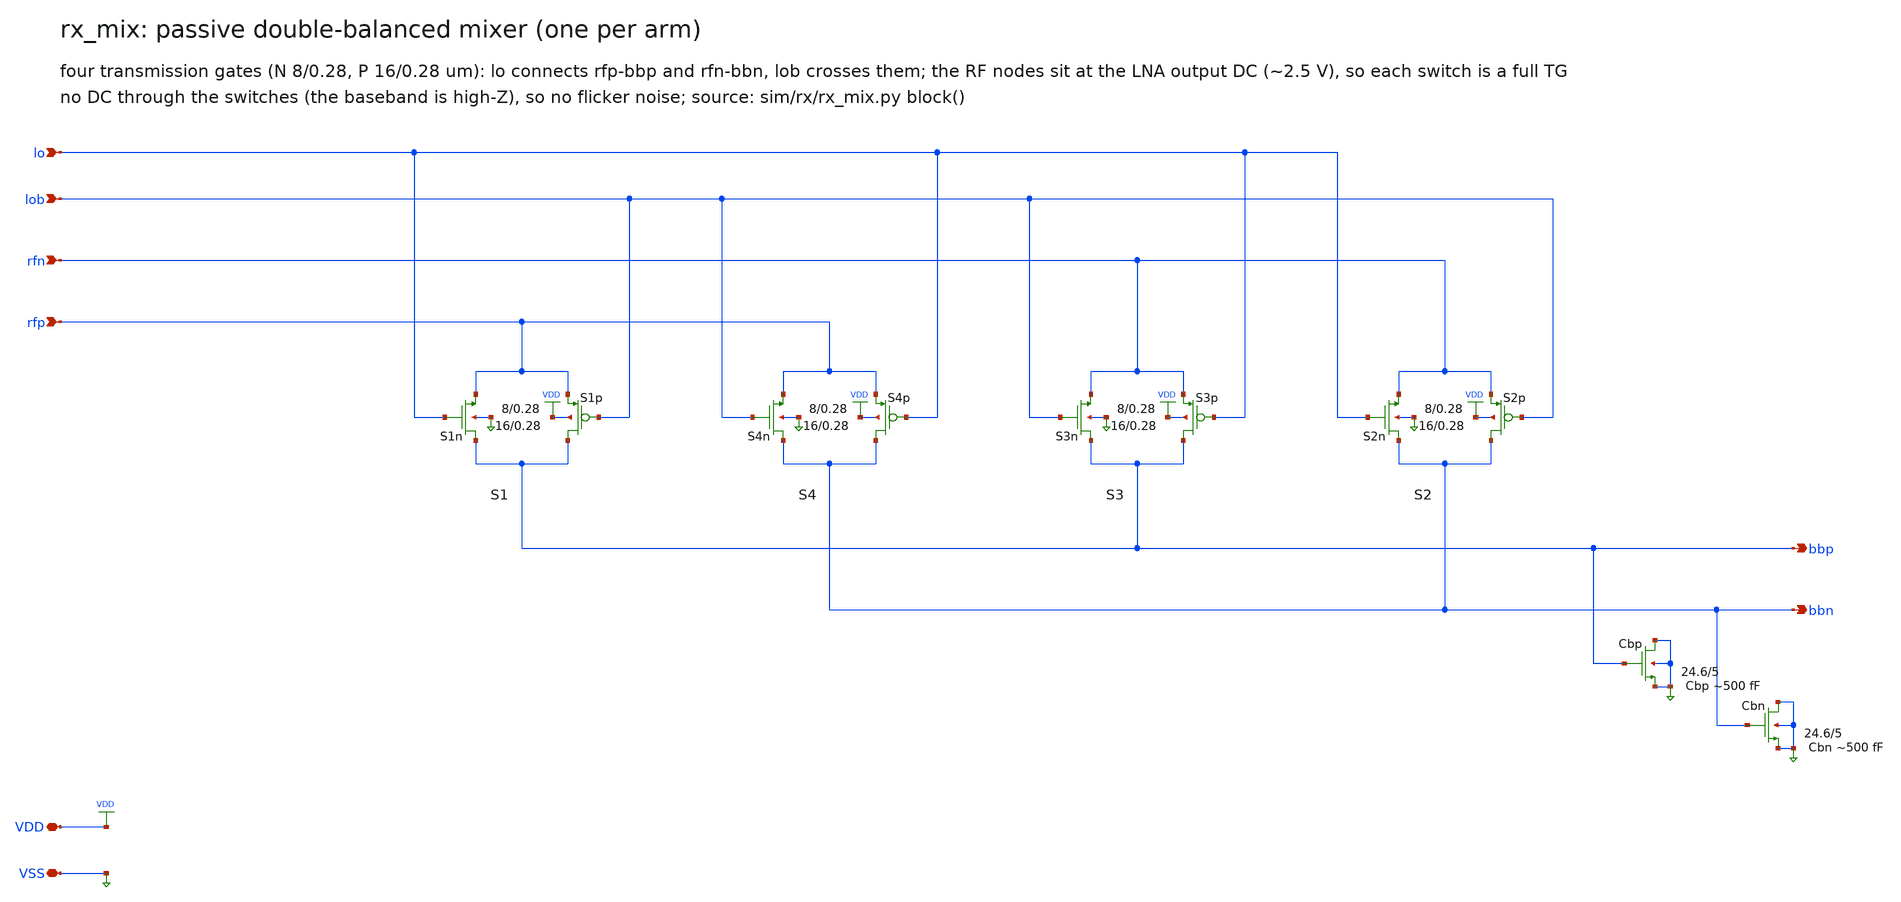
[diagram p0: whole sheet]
** sch_path: xschem/rx_mix.sch
**.subckt rx_mix VDD VSS rfp rfn bbp bbn lo lob
*.iopin VDD
*.iopin VSS
*.ipin rfp
*.ipin rfn
*.opin bbp
*.opin bbn
*.ipin lo
*.ipin lob
XS1n bbp lo rfp VSS nfet_03v3 L=0.28u W=8.0u nf=1 ad=4.0p as=4.0p pd=17.0u ps=17.0u nrd=0 nrs=0 sa=0
+ sb=0 sd=0 m=1
XS1p bbp lob rfp VDD pfet_03v3 L=0.28u W=16.0u nf=1 ad=8.0p as=8.0p pd=33.0u ps=33.0u nrd=0 nrs=0
+ sa=0 sb=0 sd=0 m=1
XS4n bbn lob rfp VSS nfet_03v3 L=0.28u W=8.0u nf=1 ad=4.0p as=4.0p pd=17.0u ps=17.0u nrd=0 nrs=0
+ sa=0 sb=0 sd=0 m=1
XS4p bbn lo rfp VDD pfet_03v3 L=0.28u W=16.0u nf=1 ad=8.0p as=8.0p pd=33.0u ps=33.0u nrd=0 nrs=0
+ sa=0 sb=0 sd=0 m=1
XS3n bbp lob rfn VSS nfet_03v3 L=0.28u W=8.0u nf=1 ad=4.0p as=4.0p pd=17.0u ps=17.0u nrd=0 nrs=0
+ sa=0 sb=0 sd=0 m=1
XS3p bbp lo rfn VDD pfet_03v3 L=0.28u W=16.0u nf=1 ad=8.0p as=8.0p pd=33.0u ps=33.0u nrd=0 nrs=0
+ sa=0 sb=0 sd=0 m=1
XS2n bbn lo rfn VSS nfet_03v3 L=0.28u W=8.0u nf=1 ad=4.0p as=4.0p pd=17.0u ps=17.0u nrd=0 nrs=0 sa=0
+ sb=0 sd=0 m=1
XS2p bbn lob rfn VDD pfet_03v3 L=0.28u W=16.0u nf=1 ad=8.0p as=8.0p pd=33.0u ps=33.0u nrd=0 nrs=0
+ sa=0 sb=0 sd=0 m=1
XCbp VSS bbp VSS VSS nfet_03v3 L=5.0u W=24.57u nf=1 ad=12.285p as=12.285p pd=50.14u ps=50.14u nrd=0
+ nrs=0 sa=0 sb=0 sd=0 m=1
XCbn VSS bbn VSS VSS nfet_03v3 L=5.0u W=24.57u nf=1 ad=12.285p as=12.285p pd=50.14u ps=50.14u nrd=0
+ nrs=0 sa=0 sb=0 sd=0 m=1
**.ends
.end
